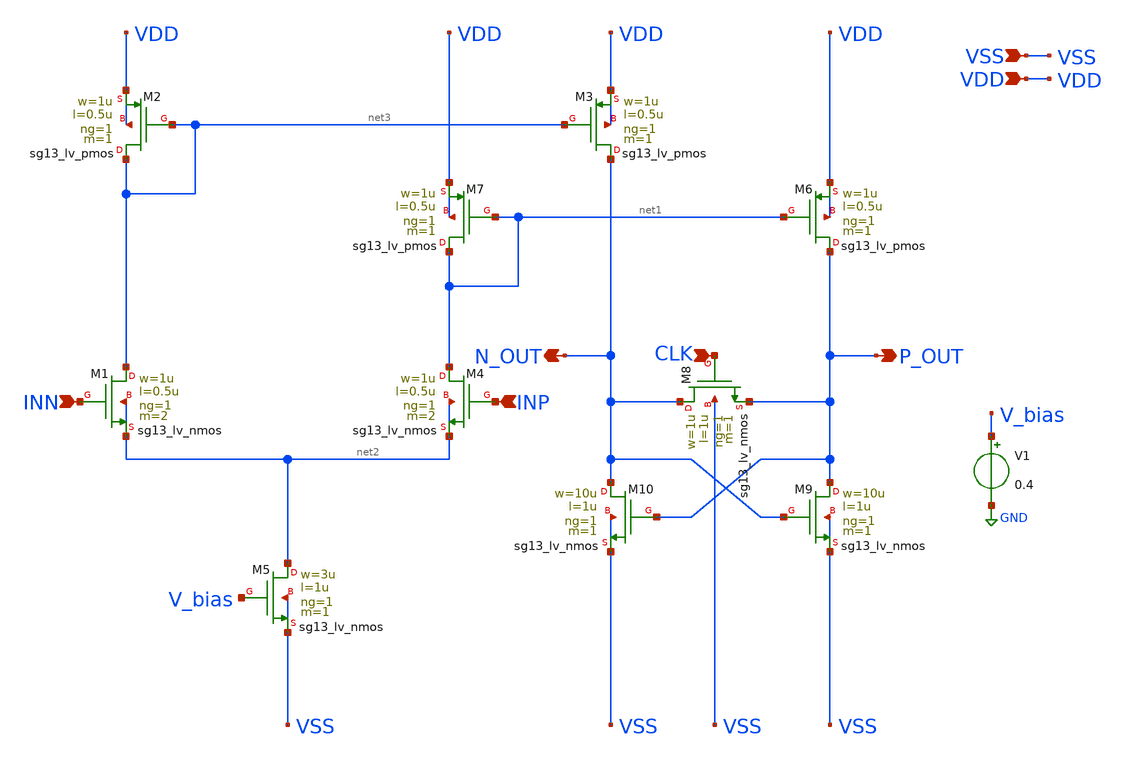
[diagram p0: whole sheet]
** sch_path: 02-signal-processing/comparator/comparator.sch
**.subckt comparator VDD VSS N_OUT P_OUT INN INP CLK
*.ipin VDD
*.ipin VSS
*.opin N_OUT
*.opin P_OUT
*.ipin INN
*.ipin INP
*.ipin CLK
XM1 net3 INN net2 net2 sg13_lv_nmos w=1u l=0.5u ng=1 m=2 mm_ok=1
XM2 net3 net3 VDD VDD sg13_lv_pmos w=1u l=0.5u ng=1 m=1 mm_ok=1
XM3 N_OUT net3 VDD VDD sg13_lv_pmos w=1u l=0.5u ng=1 m=1 mm_ok=1
XM4 net1 INP net2 net2 sg13_lv_nmos w=1u l=0.5u ng=1 m=2 mm_ok=1
XM5 net2 V_bias VSS VSS sg13_lv_nmos w=3u l=1u ng=1 m=1 mm_ok=1
XM7 net1 net1 VDD VDD sg13_lv_pmos w=1u l=0.5u ng=1 m=1 mm_ok=1
XM6 P_OUT net1 VDD VDD sg13_lv_pmos w=1u l=0.5u ng=1 m=1 mm_ok=1
XM8 N_OUT CLK P_OUT VSS sg13_lv_nmos w=1u l=1u ng=1 m=1 mm_ok=1
XM9 P_OUT N_OUT VSS VSS sg13_lv_nmos w=10u l=1u ng=1 m=1 mm_ok=1
XM10 N_OUT P_OUT VSS VSS sg13_lv_nmos w=10u l=1u ng=1 m=1 mm_ok=1
V1 V_bias GND 0.4
**.ends
.GLOBAL GND
.end
